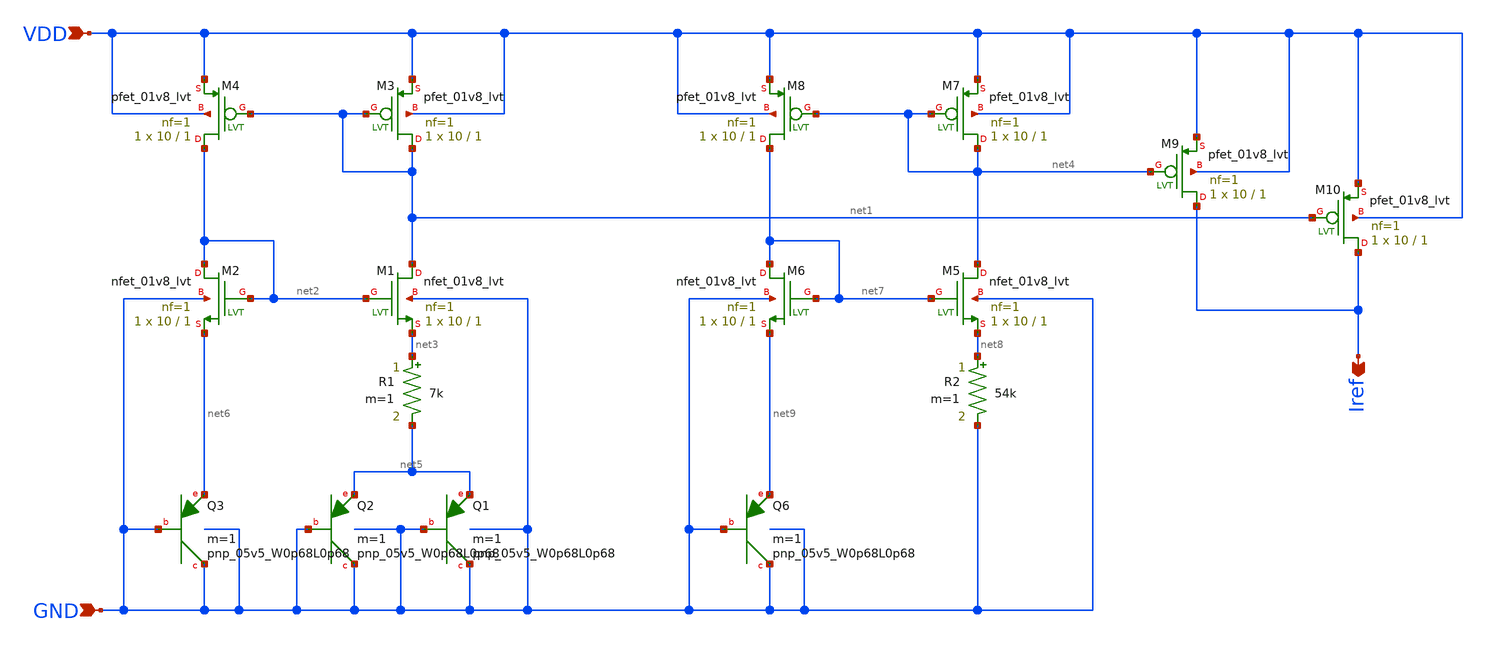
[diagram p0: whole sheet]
** sch_path: Analog_Blocks/Reference_Current/Schematic/Reference_Current.sch
**.subckt Reference_Current VDD GND Iref
*.ipin VDD
*.ipin GND
*.opin Iref
R1 net3 net5 7k m=1
XQ1 GND GND net5 sky130_fd_pr__pnp_05v5_W0p68L0p68 m=1
XQ2 GND GND net5 sky130_fd_pr__pnp_05v5_W0p68L0p68 m=1
XQ3 GND GND net6 sky130_fd_pr__pnp_05v5_W0p68L0p68 m=1
R2 net8 GND 54k m=1
XQ6 GND GND net9 sky130_fd_pr__pnp_05v5_W0p68L0p68 m=1
XM1 net1 net2 net3 GND sky130_fd_pr__nfet_01v8_lvt L=1 W=10 nf=1 ad='int((nf+1)/2) * W/nf * 0.29' as='int((nf+2)/2) * W/nf * 0.29'
+ pd='2*int((nf+1)/2) * (W/nf + 0.29)' ps='2*int((nf+2)/2) * (W/nf + 0.29)' nrd='0.29 / W' nrs='0.29 / W'
+ sa=0 sb=0 sd=0 mult=1 m=1
XM2 net2 net2 net6 GND sky130_fd_pr__nfet_01v8_lvt L=1 W=10 nf=1 ad='int((nf+1)/2) * W/nf * 0.29' as='int((nf+2)/2) * W/nf * 0.29'
+ pd='2*int((nf+1)/2) * (W/nf + 0.29)' ps='2*int((nf+2)/2) * (W/nf + 0.29)' nrd='0.29 / W' nrs='0.29 / W'
+ sa=0 sb=0 sd=0 mult=1 m=1
XM3 net1 net1 VDD VDD sky130_fd_pr__pfet_01v8_lvt L=1 W=10 nf=1 ad='int((nf+1)/2) * W/nf * 0.29' as='int((nf+2)/2) * W/nf * 0.29'
+ pd='2*int((nf+1)/2) * (W/nf + 0.29)' ps='2*int((nf+2)/2) * (W/nf + 0.29)' nrd='0.29 / W' nrs='0.29 / W'
+ sa=0 sb=0 sd=0 mult=1 m=1
XM4 net2 net1 VDD VDD sky130_fd_pr__pfet_01v8_lvt L=1 W=10 nf=1 ad='int((nf+1)/2) * W/nf * 0.29' as='int((nf+2)/2) * W/nf * 0.29'
+ pd='2*int((nf+1)/2) * (W/nf + 0.29)' ps='2*int((nf+2)/2) * (W/nf + 0.29)' nrd='0.29 / W' nrs='0.29 / W'
+ sa=0 sb=0 sd=0 mult=1 m=1
XM5 net4 net7 net8 GND sky130_fd_pr__nfet_01v8_lvt L=1 W=10 nf=1 ad='int((nf+1)/2) * W/nf * 0.29' as='int((nf+2)/2) * W/nf * 0.29'
+ pd='2*int((nf+1)/2) * (W/nf + 0.29)' ps='2*int((nf+2)/2) * (W/nf + 0.29)' nrd='0.29 / W' nrs='0.29 / W'
+ sa=0 sb=0 sd=0 mult=1 m=1
XM6 net7 net7 net9 GND sky130_fd_pr__nfet_01v8_lvt L=1 W=10 nf=1 ad='int((nf+1)/2) * W/nf * 0.29' as='int((nf+2)/2) * W/nf * 0.29'
+ pd='2*int((nf+1)/2) * (W/nf + 0.29)' ps='2*int((nf+2)/2) * (W/nf + 0.29)' nrd='0.29 / W' nrs='0.29 / W'
+ sa=0 sb=0 sd=0 mult=1 m=1
XM7 net4 net4 VDD VDD sky130_fd_pr__pfet_01v8_lvt L=1 W=10 nf=1 ad='int((nf+1)/2) * W/nf * 0.29' as='int((nf+2)/2) * W/nf * 0.29'
+ pd='2*int((nf+1)/2) * (W/nf + 0.29)' ps='2*int((nf+2)/2) * (W/nf + 0.29)' nrd='0.29 / W' nrs='0.29 / W'
+ sa=0 sb=0 sd=0 mult=1 m=1
XM8 net7 net4 VDD VDD sky130_fd_pr__pfet_01v8_lvt L=1 W=10 nf=1 ad='int((nf+1)/2) * W/nf * 0.29' as='int((nf+2)/2) * W/nf * 0.29'
+ pd='2*int((nf+1)/2) * (W/nf + 0.29)' ps='2*int((nf+2)/2) * (W/nf + 0.29)' nrd='0.29 / W' nrs='0.29 / W'
+ sa=0 sb=0 sd=0 mult=1 m=1
XM9 Iref net4 VDD VDD sky130_fd_pr__pfet_01v8_lvt L=1 W=10 nf=1 ad='int((nf+1)/2) * W/nf * 0.29' as='int((nf+2)/2) * W/nf * 0.29'
+ pd='2*int((nf+1)/2) * (W/nf + 0.29)' ps='2*int((nf+2)/2) * (W/nf + 0.29)' nrd='0.29 / W' nrs='0.29 / W'
+ sa=0 sb=0 sd=0 mult=1 m=1
XM10 Iref net1 VDD VDD sky130_fd_pr__pfet_01v8_lvt L=1 W=10 nf=1 ad='int((nf+1)/2) * W/nf * 0.29' as='int((nf+2)/2) * W/nf * 0.29'
+ pd='2*int((nf+1)/2) * (W/nf + 0.29)' ps='2*int((nf+2)/2) * (W/nf + 0.29)' nrd='0.29 / W' nrs='0.29 / W'
+ sa=0 sb=0 sd=0 mult=1 m=1
**.ends
.end
